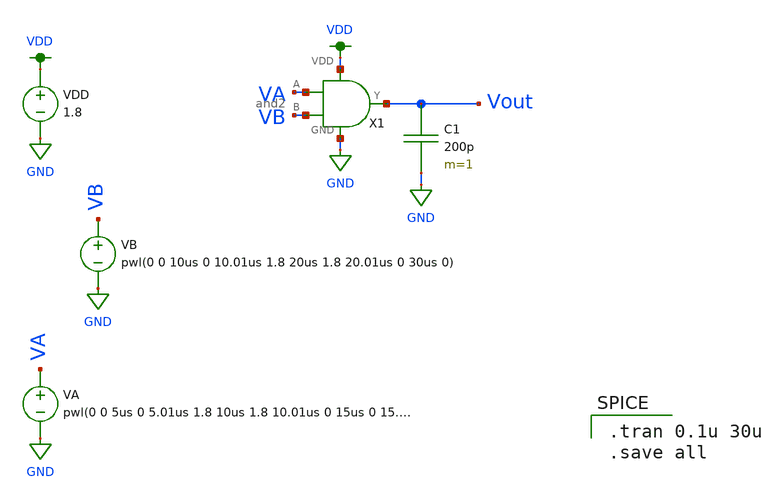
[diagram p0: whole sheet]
** sch_path: schematic/layout_driven_schematics/and2_schematic_simulation.sch
**.subckt and2_schematic_simulation
C1 Vout GND 200p m=1
VDD VDD GND 1.8
VA VA GND pwl(0 0 5us 0 5.01us 1.8 10us 1.8 10.01us 0 15us 0 15.1us 1.8 20us 1.8 20.01us 0 30us 0)
VB VB GND pwl(0 0 10us 0 10.01us 1.8 20us 1.8 20.01us 0 30us 0)
X1 VDD VA GND Vout VB and2
**** begin user architecture code

.option wnflag=1
.lib ~/skywater/skywater-pdk/libraries/sky130_fd_pr_ngspice/latest/models/sky130.lib.spice tt


.tran 0.1u 30u
.save all

**** end user architecture code
**.ends

* expanding   symbol:  /home/madvlsi/Documents/MP1/schematic/layout_driven_schematics/and2.sym # of
*+ pins=5
** sym_path: schematic/layout_driven_schematics/and2.sym
** sch_path: schematic/layout_driven_schematics/and2.sch
.subckt and2 VDD A GND Y B
*.ipin A
*.ipin B
*.opin Y
*.iopin VDD
*.iopin GND
X1 A B net1 VDD GND nand2
X2 net1 Y VDD GND inverter
.ends


* expanding   symbol:  /home/madvlsi/Documents/MP1/schematic/layout_driven_schematics/nand2.sym # of
*+ pins=5
** sym_path: schematic/layout_driven_schematics/nand2.sym
** sch_path: schematic/layout_driven_schematics/nand2.sch
.subckt nand2 A B Y VDD GND
*.ipin A
*.opin Y
*.ipin B
*.iopin VDD
*.iopin VDD
*.iopin GND
XM5 Y A VDD VDD sky130_fd_pr__pfet_01v8 L=0.15 W=2 nf=1 ad='int((nf+1)/2) * W/nf * 0.29' as='int((nf+2)/2) * W/nf * 0.29'
+ pd='2*int((nf+1)/2) * (W/nf + 0.29)' ps='2*int((nf+2)/2) * (W/nf + 0.29)' nrd='0.29 / W' nrs='0.29 / W'
+ sa=0 sb=0 sd=0 mult=1 m=1
XM6 VDD B Y VDD sky130_fd_pr__pfet_01v8 L=0.15 W=2 nf=1 ad='int((nf+1)/2) * W/nf * 0.29' as='int((nf+2)/2) * W/nf * 0.29'
+ pd='2*int((nf+1)/2) * (W/nf + 0.29)' ps='2*int((nf+2)/2) * (W/nf + 0.29)' nrd='0.29 / W' nrs='0.29 / W'
+ sa=0 sb=0 sd=0 mult=1 m=1
XM7 GND A net1 GND sky130_fd_pr__nfet_01v8 L=0.15 W=2 nf=1 ad='int((nf+1)/2) * W/nf * 0.29' as='int((nf+2)/2) * W/nf * 0.29'
+ pd='2*int((nf+1)/2) * (W/nf + 0.29)' ps='2*int((nf+2)/2) * (W/nf + 0.29)' nrd='0.29 / W' nrs='0.29 / W'
+ sa=0 sb=0 sd=0 mult=1 m=1
XM8 net1 B Y GND sky130_fd_pr__nfet_01v8 L=0.15 W=2 nf=1 ad='int((nf+1)/2) * W/nf * 0.29' as='int((nf+2)/2) * W/nf * 0.29'
+ pd='2*int((nf+1)/2) * (W/nf + 0.29)' ps='2*int((nf+2)/2) * (W/nf + 0.29)' nrd='0.29 / W' nrs='0.29 / W'
+ sa=0 sb=0 sd=0 mult=1 m=1
.ends


* expanding   symbol:  /home/madvlsi/Documents/MP1/schematic/layout_driven_schematics/inverter.sym #
*+ of pins=4
** sym_path: schematic/layout_driven_schematics/inverter.sym
** sch_path: schematic/layout_driven_schematics/inverter.sch
.subckt inverter A Y VDD GND
*.ipin A
*.iopin VDD
*.iopin GND
*.opin Y
XM3 Y A VDD VDD sky130_fd_pr__pfet_01v8 L=0.15 W=2 nf=1 ad='int((nf+1)/2) * W/nf * 0.29' as='int((nf+2)/2) * W/nf * 0.29'
+ pd='2*int((nf+1)/2) * (W/nf + 0.29)' ps='2*int((nf+2)/2) * (W/nf + 0.29)' nrd='0.29 / W' nrs='0.29 / W'
+ sa=0 sb=0 sd=0 mult=1 m=1
XM4 GND A Y GND sky130_fd_pr__nfet_01v8 L=0.15 W=2 nf=1 ad='int((nf+1)/2) * W/nf * 0.29' as='int((nf+2)/2) * W/nf * 0.29'
+ pd='2*int((nf+1)/2) * (W/nf + 0.29)' ps='2*int((nf+2)/2) * (W/nf + 0.29)' nrd='0.29 / W' nrs='0.29 / W'
+ sa=0 sb=0 sd=0 mult=1 m=1
.ends

.GLOBAL GND
.GLOBAL VDD
.end
